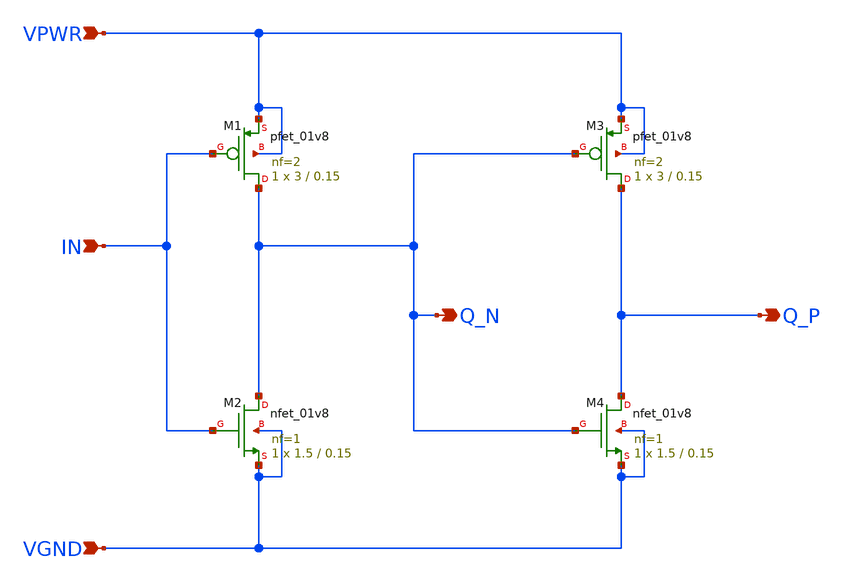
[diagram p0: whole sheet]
** sch_path: swtch_twoinv_sky130nm/design/SWTCH_TWOINV_SKY130NM/SWTCH_TWOINV.sch
**.subckt SWTCH_TWOINV VPWR VGND IN Q_P Q_N
*.ipin VPWR
*.ipin VGND
*.ipin IN
*.opin Q_P
*.opin Q_N
XM1 Q_N IN VPWR VPWR sky130_fd_pr__pfet_01v8 L=0.15 W=3 nf=2 ad='int((nf+1)/2) * W/nf * 0.29' as='int((nf+2)/2) * W/nf * 0.29'
+ pd='2*int((nf+1)/2) * (W/nf + 0.29)' ps='2*int((nf+2)/2) * (W/nf + 0.29)' nrd='0.29 / W' nrs='0.29 / W'
+ sa=0 sb=0 sd=0 mult=1 m=1
XM2 Q_N IN VGND VGND sky130_fd_pr__nfet_01v8 L=0.15 W=1.5 nf=1 ad='int((nf+1)/2) * W/nf * 0.29' as='int((nf+2)/2) * W/nf * 0.29'
+ pd='2*int((nf+1)/2) * (W/nf + 0.29)' ps='2*int((nf+2)/2) * (W/nf + 0.29)' nrd='0.29 / W' nrs='0.29 / W'
+ sa=0 sb=0 sd=0 mult=1 m=1
XM3 Q_P Q_N VPWR VPWR sky130_fd_pr__pfet_01v8 L=0.15 W=3 nf=2 ad='int((nf+1)/2) * W/nf * 0.29' as='int((nf+2)/2) * W/nf * 0.29'
+ pd='2*int((nf+1)/2) * (W/nf + 0.29)' ps='2*int((nf+2)/2) * (W/nf + 0.29)' nrd='0.29 / W' nrs='0.29 / W'
+ sa=0 sb=0 sd=0 mult=1 m=1
XM4 Q_P Q_N VGND VGND sky130_fd_pr__nfet_01v8 L=0.15 W=1.5 nf=1 ad='int((nf+1)/2) * W/nf * 0.29' as='int((nf+2)/2) * W/nf * 0.29'
+ pd='2*int((nf+1)/2) * (W/nf + 0.29)' ps='2*int((nf+2)/2) * (W/nf + 0.29)' nrd='0.29 / W' nrs='0.29 / W'
+ sa=0 sb=0 sd=0 mult=1 m=1
**.ends
.end
